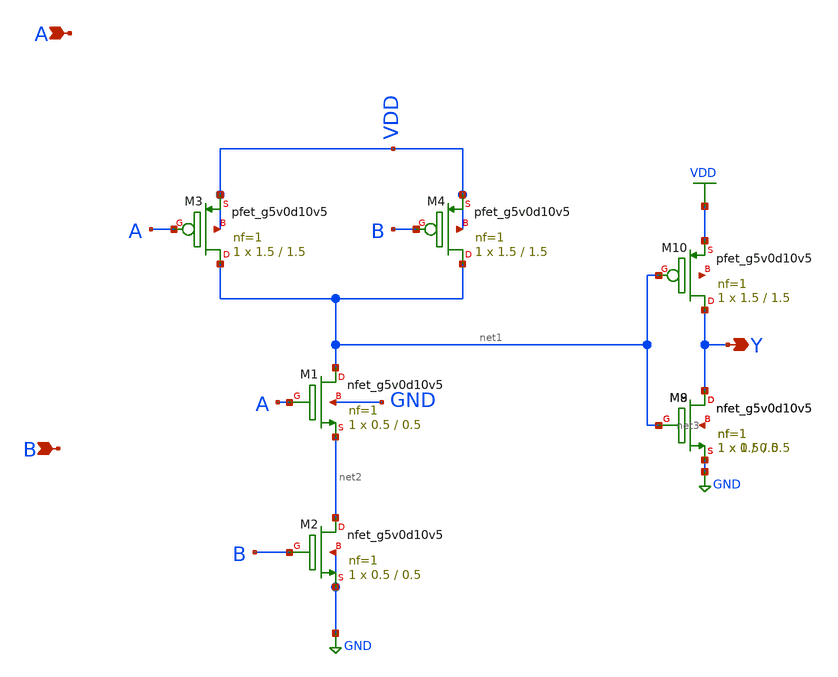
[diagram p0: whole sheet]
** sch_path: xschem/StandardCells/AND2.sch
**.subckt AND2 A B Y
*.ipin A
*.ipin B
*.opin Y
XM1 net1 A net2 GND sky130_fd_pr__nfet_g5v0d10v5 L=0.5 W=0.5 nf=1 ad='int((nf+1)/2) * W/nf * 0.29' as='int((nf+2)/2) * W/nf * 0.29'
+ pd='2*int((nf+1)/2) * (W/nf + 0.29)' ps='2*int((nf+2)/2) * (W/nf + 0.29)' nrd='0.29 / W' nrs='0.29 / W'
+ sa=0 sb=0 sd=0 mult=1 m=1
XM2 net2 B GND GND sky130_fd_pr__nfet_g5v0d10v5 L=0.5 W=0.5 nf=1 ad='int((nf+1)/2) * W/nf * 0.29' as='int((nf+2)/2) * W/nf * 0.29'
+ pd='2*int((nf+1)/2) * (W/nf + 0.29)' ps='2*int((nf+2)/2) * (W/nf + 0.29)' nrd='0.29 / W' nrs='0.29 / W'
+ sa=0 sb=0 sd=0 mult=1 m=1
XM3 net1 A VDD VDD sky130_fd_pr__pfet_g5v0d10v5 L=1.5 W=1.5 nf=1 ad='int((nf+1)/2) * W/nf * 0.29' as='int((nf+2)/2) * W/nf * 0.29'
+ pd='2*int((nf+1)/2) * (W/nf + 0.29)' ps='2*int((nf+2)/2) * (W/nf + 0.29)' nrd='0.29 / W' nrs='0.29 / W'
+ sa=0 sb=0 sd=0 mult=1 m=1
XM4 net1 B VDD VDD sky130_fd_pr__pfet_g5v0d10v5 L=1.5 W=1.5 nf=1 ad='int((nf+1)/2) * W/nf * 0.29' as='int((nf+2)/2) * W/nf * 0.29'
+ pd='2*int((nf+1)/2) * (W/nf + 0.29)' ps='2*int((nf+2)/2) * (W/nf + 0.29)' nrd='0.29 / W' nrs='0.29 / W'
+ sa=0 sb=0 sd=0 mult=1 m=1
XM8 Y net1 GND net3 sky130_fd_pr__nfet_g5v0d10v5 L=0.5 W=0.5 nf=1 ad='int((nf+1)/2) * W/nf * 0.29' as='int((nf+2)/2) * W/nf * 0.29'
+ pd='2*int((nf+1)/2) * (W/nf + 0.29)' ps='2*int((nf+2)/2) * (W/nf + 0.29)' nrd='0.29 / W' nrs='0.29 / W'
+ sa=0 sb=0 sd=0 mult=1 m=1
XM9 Y net1 GND net3 sky130_fd_pr__nfet_g5v0d10v5 L=0.5 W=1 nf=1 ad='int((nf+1)/2) * W/nf * 0.29' as='int((nf+2)/2) * W/nf * 0.29'
+ pd='2*int((nf+1)/2) * (W/nf + 0.29)' ps='2*int((nf+2)/2) * (W/nf + 0.29)' nrd='0.29 / W' nrs='0.29 / W'
+ sa=0 sb=0 sd=0 mult=1 m=1
XM10 Y net1 VDD net4 sky130_fd_pr__pfet_g5v0d10v5 L=1.5 W=1.5 nf=1 ad='int((nf+1)/2) * W/nf * 0.29' as='int((nf+2)/2) * W/nf * 0.29'
+ pd='2*int((nf+1)/2) * (W/nf + 0.29)' ps='2*int((nf+2)/2) * (W/nf + 0.29)' nrd='0.29 / W' nrs='0.29 / W'
+ sa=0 sb=0 sd=0 mult=1 m=1
**.ends
.GLOBAL GND
.GLOBAL VDD
.end
